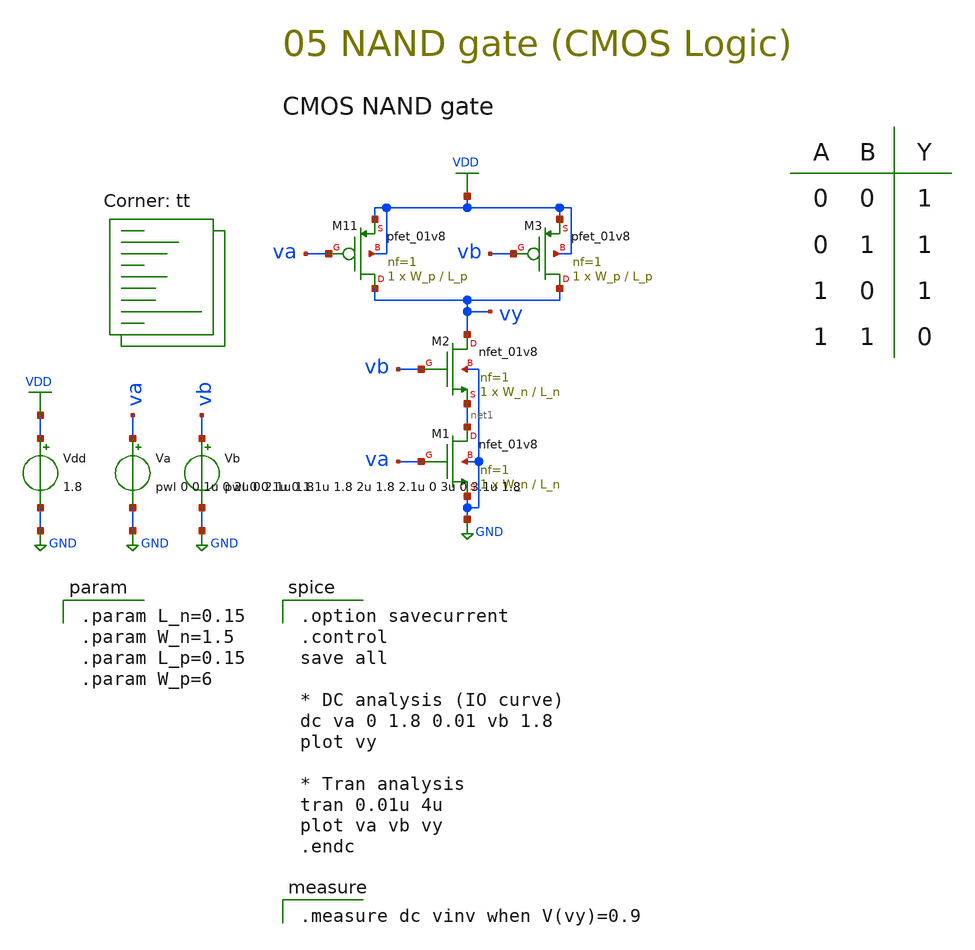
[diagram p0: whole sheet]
** sch_path: 05-b_NAND_CMOS.sch
**.subckt 05-b_NAND_CMOS
Vdd VDD GND 1.8
XM1 net1 va GND GND sky130_fd_pr__nfet_01v8 L=L_n W=W_n nf=1 ad='int((1 + 1)/2) * W_n / 1 * 0.29' as='int((1 + 2)/2) * W_n / 1 * 0.29'
+ pd='2*int((1 + 1)/2) * (W_n / 1 + 0.29)' ps='2*int((1 + 2)/2) * (W_n / 1 + 0.29)' nrd='0.29 / W_n ' nrs='0.29 / W_n '
+ sa=0 sb=0 sd=0 mult=1 m=1
XM2 vy vb net1 GND sky130_fd_pr__nfet_01v8 L=L_n W=W_n nf=1 ad='int((1 + 1)/2) * W_n / 1 * 0.29' as='int((1 + 2)/2) * W_n / 1 * 0.29'
+ pd='2*int((1 + 1)/2) * (W_n / 1 + 0.29)' ps='2*int((1 + 2)/2) * (W_n / 1 + 0.29)' nrd='0.29 / W_n ' nrs='0.29 / W_n '
+ sa=0 sb=0 sd=0 mult=1 m=1
Va va GND pwl 0 0 1u 0 2u 0 2.1u 1.8
Vb vb GND pwl 0 0 1u 0 1.1u 1.8 2u 1.8 2.1u 0 3u 0 3.1u 1.8
XM11 vy va VDD VDD sky130_fd_pr__pfet_01v8 L=L_p W=W_p nf=1 ad='int((nf+1)/2) * W/nf * 0.29' as='int((nf+2)/2) * W/nf * 0.29'
+ pd='2*int((nf+1)/2) * (W/nf + 0.29)' ps='2*int((nf+2)/2) * (W/nf + 0.29)' nrd='0.29 / W' nrs='0.29 / W'
+ sa=0 sb=0 sd=0 mult=1 m=1
XM3 vy vb VDD VDD sky130_fd_pr__pfet_01v8 L=L_p W=W_p nf=1 ad='int((nf+1)/2) * W/nf * 0.29' as='int((nf+2)/2) * W/nf * 0.29'
+ pd='2*int((nf+1)/2) * (W/nf + 0.29)' ps='2*int((nf+2)/2) * (W/nf + 0.29)' nrd='0.29 / W' nrs='0.29 / W'
+ sa=0 sb=0 sd=0 mult=1 m=1
**** begin user architecture code
.lib $::SKYWATER_MODELS/sky130.lib.spice tt

.param L_n=0.15
.param W_n=1.5
.param L_p=0.15
.param W_p=6


.option savecurrent
.control
save all

* DC analysis (IO curve)
dc va 0 1.8 0.01 vb 1.8
plot vy

* Tran analysis
tran 0.01u 4u
plot va vb vy
.endc


.measure dc vinv when V(vy)=0.9

**** end user architecture code
**.ends
.GLOBAL GND
.GLOBAL VDD
.end
